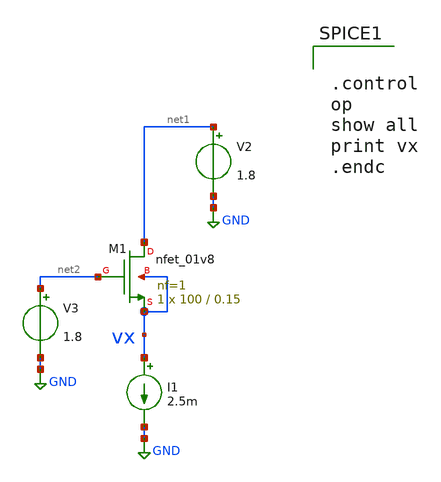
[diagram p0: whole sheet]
** sch_path: mos_sizing/nmos_gm_fix.sch
**.subckt nmos_gm_fix
XM1 net1 net2 vx vx sky130_fd_pr__nfet_01v8 L=0.15 W=100 nf=1 ad='int((nf+1)/2) * W/nf * 0.29' as='int((nf+2)/2) * W/nf * 0.29'
+ pd='2*int((nf+1)/2) * (W/nf + 0.29)' ps='2*int((nf+2)/2) * (W/nf + 0.29)' nrd='0.29 / W' nrs='0.29 / W'
+ sa=0 sb=0 sd=0 mult=1 m=1
I1 vx GND 2.5m
V2 net1 GND 1.8
V3 net2 GND 1.8
**** begin user architecture code


.option wnflag = 1
.lib /usr/local/share/pdk/sky130A/libs.tech/ngspice/sky130.lib.spice tt
.include /usr/local/share/pdk/sky130A/libs.ref/sky130_fd_pr/spice/sky130_fd_pr__ind_05_220.model.spice
.param mc_mm_switch=0




.control
op
show all
print vx
.endc


**** end user architecture code
**.ends
.GLOBAL GND
.end
